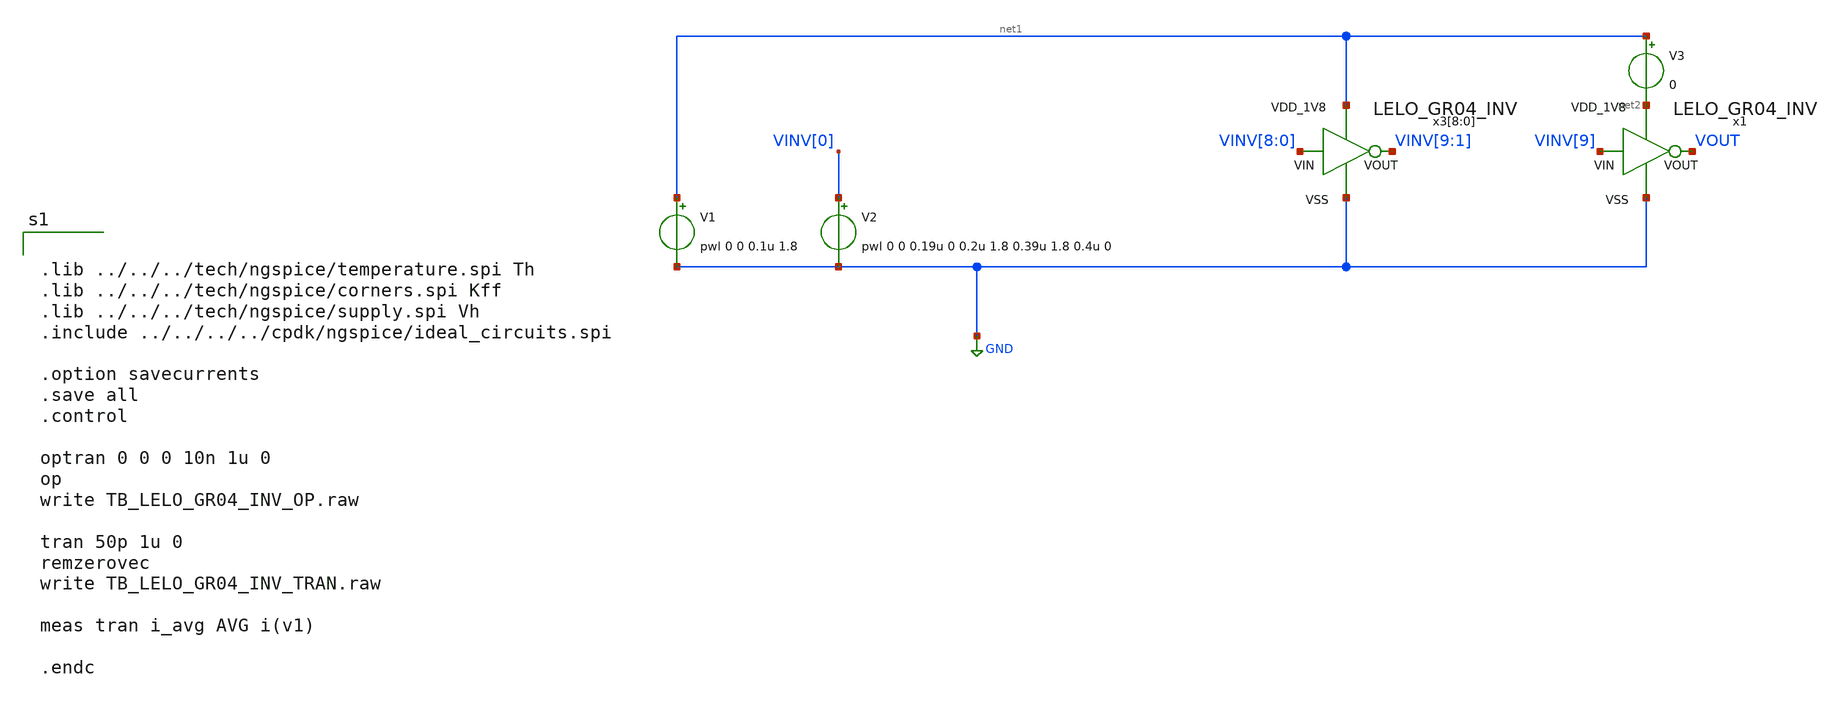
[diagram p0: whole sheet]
** sch_path: design/LELO_GR04_SKY130A/TB_LELO_GR04_INV.sch
**.subckt TB_LELO_GR04_INV
V1 net1 GND pwl 0 0 0.1u 1.8
V2 VINV[0] GND pwl 0 0 0.19u 0 0.2u 1.8 0.39u 1.8 0.4u 0
x3[8] net1 VINV[8] VINV[9] GND LELO_GR04_INV
x3[7] net1 VINV[7] VINV[8] GND LELO_GR04_INV
x3[6] net1 VINV[6] VINV[7] GND LELO_GR04_INV
x3[5] net1 VINV[5] VINV[6] GND LELO_GR04_INV
x3[4] net1 VINV[4] VINV[5] GND LELO_GR04_INV
x3[3] net1 VINV[3] VINV[4] GND LELO_GR04_INV
x3[2] net1 VINV[2] VINV[3] GND LELO_GR04_INV
x3[1] net1 VINV[1] VINV[2] GND LELO_GR04_INV
x3[0] net1 VINV[0] VINV[1] GND LELO_GR04_INV
V3 net1 net2 0
x1 net2 VINV[9] VOUT GND LELO_GR04_INV
**** begin user architecture code


.lib ../../../tech/ngspice/temperature.spi Th
.lib ../../../tech/ngspice/corners.spi Kff
.lib ../../../tech/ngspice/supply.spi Vh
.include ../../../../cpdk/ngspice/ideal_circuits.spi

.option savecurrents
.save all
.control

optran 0 0 0 10n 1u 0
op
write TB_LELO_GR04_INV_OP.raw

tran 50p 1u 0
remzerovec
write TB_LELO_GR04_INV_TRAN.raw

meas tran i_avg AVG i(v1)

.endc


**** end user architecture code
**.ends
.GLOBAL GND
.end
